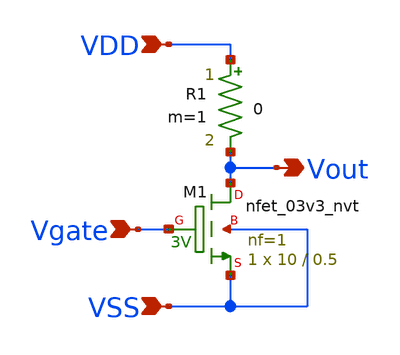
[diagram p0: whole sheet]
** sch_path: design/THESIS_EXP_RO_INVERTER_SKY130A/INV_NVT_R.sch
**.subckt INV_NVT_R VDD VSS Vgate Vout
*.ipin VDD
*.ipin VSS
*.ipin Vgate
*.opin Vout
R1 VDD Vout 0 m=1
XM1 Vout Vgate VSS VSS sky130_fd_pr__nfet_03v3_nvt L=0.5 W=10 nf=1 ad='int((nf+1)/2) * W/nf * 0.29' as='int((nf+2)/2) * W/nf * 0.29'
+ pd='2*int((nf+1)/2) * (W/nf + 0.29)' ps='2*int((nf+2)/2) * (W/nf + 0.29)' nrd='0.29 / W' nrs='0.29 / W'
+ sa=0 sb=0 sd=0 mult=1 m=1
**.ends
.end
